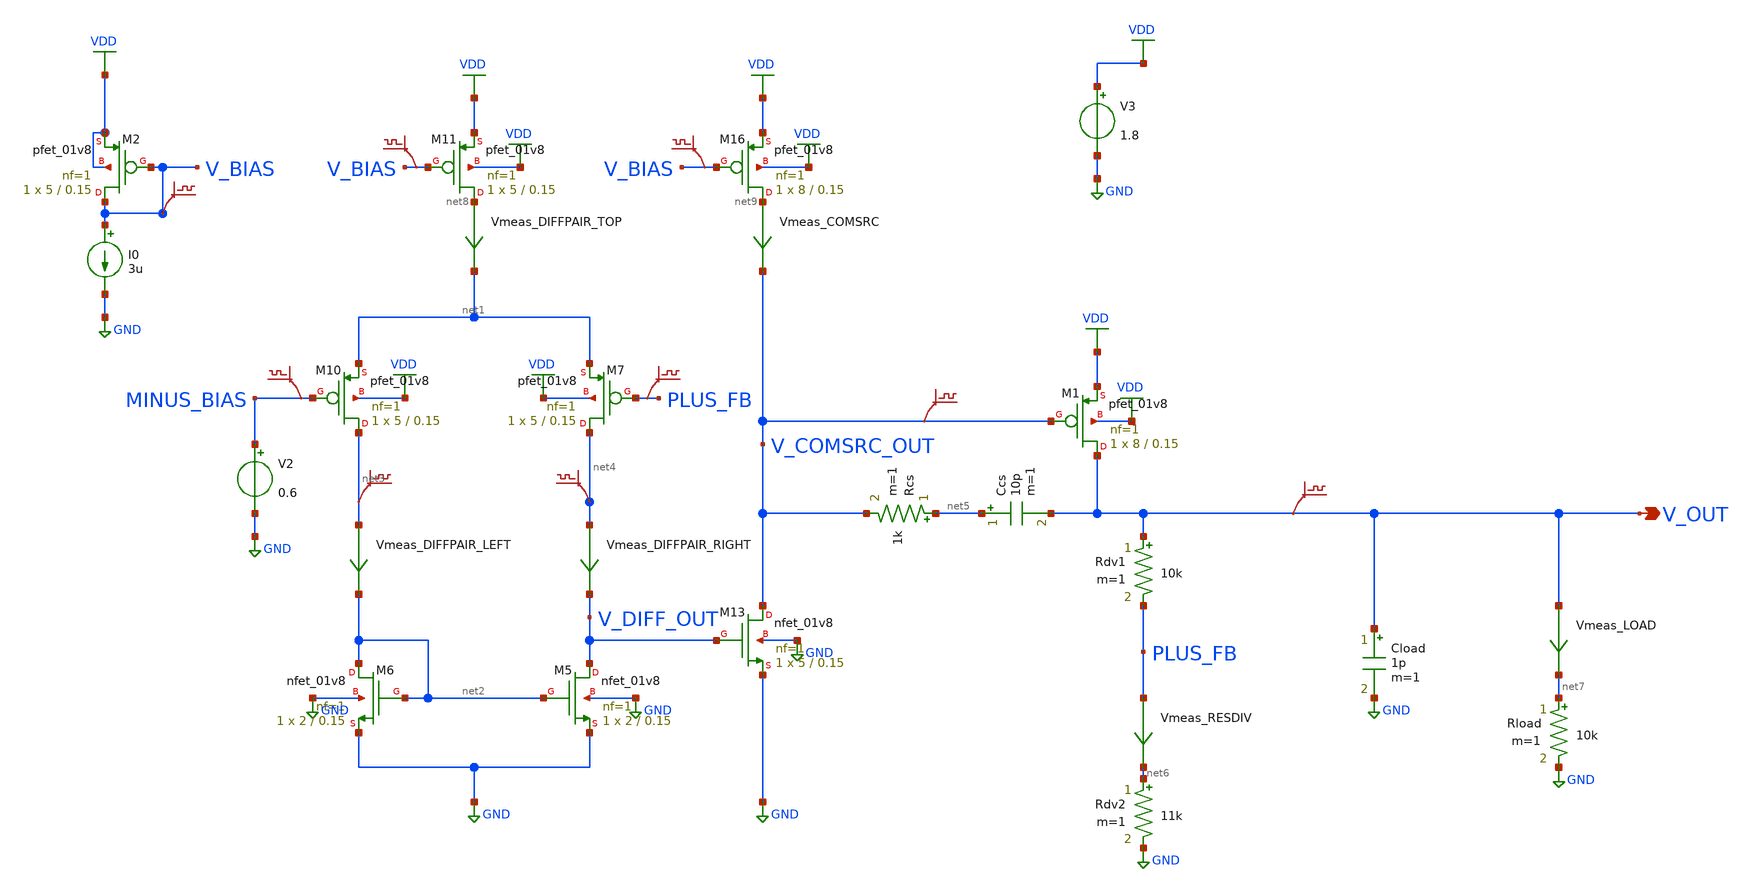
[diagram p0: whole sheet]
** sch_path: lib/xschem/LDO/LDO.sch
**.subckt LDO V_OUT
*.opin V_OUT
XM6 net2 net2 GND GND sky130_fd_pr__nfet_01v8 L=0.15 W=2 nf=1 ad='int((nf+1)/2) * W/nf * 0.29' as='int((nf+2)/2) * W/nf * 0.29'
+ pd='2*int((nf+1)/2) * (W/nf + 0.29)' ps='2*int((nf+2)/2) * (W/nf + 0.29)' nrd='0.29 / W' nrs='0.29 / W'
+ sa=0 sb=0 sd=0 mult=1 m=1
XM5 V_DIFF_OUT net2 GND GND sky130_fd_pr__nfet_01v8 L=0.15 W=2 nf=1 ad='int((nf+1)/2) * W/nf * 0.29'
+ as='int((nf+2)/2) * W/nf * 0.29' pd='2*int((nf+1)/2) * (W/nf + 0.29)' ps='2*int((nf+2)/2) * (W/nf + 0.29)'
+ nrd='0.29 / W' nrs='0.29 / W' sa=0 sb=0 sd=0 mult=1 m=1
XM7 net4 PLUS_FB net1 VDD sky130_fd_pr__pfet_01v8 L=0.15 W=5 nf=1 ad='int((nf+1)/2) * W/nf * 0.29' as='int((nf+2)/2) * W/nf * 0.29'
+ pd='2*int((nf+1)/2) * (W/nf + 0.29)' ps='2*int((nf+2)/2) * (W/nf + 0.29)' nrd='0.29 / W' nrs='0.29 / W'
+ sa=0 sb=0 sd=0 mult=1 m=1
XM10 net3 MINUS_BIAS net1 VDD sky130_fd_pr__pfet_01v8 L=0.15 W=5 nf=1 ad='int((nf+1)/2) * W/nf * 0.29'
+ as='int((nf+2)/2) * W/nf * 0.29' pd='2*int((nf+1)/2) * (W/nf + 0.29)' ps='2*int((nf+2)/2) * (W/nf + 0.29)'
+ nrd='0.29 / W' nrs='0.29 / W' sa=0 sb=0 sd=0 mult=1 m=1
XM11 net8 V_BIAS VDD VDD sky130_fd_pr__pfet_01v8 L=0.15 W=5 nf=1 ad='int((nf+1)/2) * W/nf * 0.29' as='int((nf+2)/2) * W/nf * 0.29'
+ pd='2*int((nf+1)/2) * (W/nf + 0.29)' ps='2*int((nf+2)/2) * (W/nf + 0.29)' nrd='0.29 / W' nrs='0.29 / W'
+ sa=0 sb=0 sd=0 mult=1 m=1
XM13 V_COMSRC_OUT V_DIFF_OUT GND GND sky130_fd_pr__nfet_01v8 L=0.15 W=5 nf=1 ad='int((nf+1)/2) * W/nf * 0.29'
+ as='int((nf+2)/2) * W/nf * 0.29' pd='2*int((nf+1)/2) * (W/nf + 0.29)' ps='2*int((nf+2)/2) * (W/nf + 0.29)'
+ nrd='0.29 / W' nrs='0.29 / W' sa=0 sb=0 sd=0 mult=1 m=1
XM16 net9 V_BIAS VDD VDD sky130_fd_pr__pfet_01v8 L=0.15 W=8 nf=1 ad='int((nf+1)/2) * W/nf * 0.29' as='int((nf+2)/2) * W/nf * 0.29'
+ pd='2*int((nf+1)/2) * (W/nf + 0.29)' ps='2*int((nf+2)/2) * (W/nf + 0.29)' nrd='0.29 / W' nrs='0.29 / W'
+ sa=0 sb=0 sd=0 mult=1 m=1
V2 MINUS_BIAS GND 0.6
V3 VDD GND 1.8
.save v(plus_fb)
.save v(minus_bias)
.save v(net4)
.save v(net3)
.save v(v_comsrc_out)
Vmeas_DIFFPAIR_LEFT net3 net2 0
.save i(vmeas_diffpair_left)
Vmeas_DIFFPAIR_RIGHT net4 V_DIFF_OUT 0
.save i(vmeas_diffpair_right)
Vmeas_COMSRC net9 V_COMSRC_OUT 0
.save i(vmeas_comsrc)
.save v(v_bias)
.save v(v_bias)
Rdv1 V_OUT PLUS_FB 10k m=1
Rdv2 net6 GND 11k m=1
Vmeas_RESDIV PLUS_FB net6 0
.save i(vmeas_resdiv)
Vmeas_DIFFPAIR_TOP net8 net1 0
.save i(vmeas_diffpair_top)
XM2 V_BIAS V_BIAS VDD VDD sky130_fd_pr__pfet_01v8 L=0.15 W=5 nf=1 ad='int((nf+1)/2) * W/nf * 0.29' as='int((nf+2)/2) * W/nf * 0.29'
+ pd='2*int((nf+1)/2) * (W/nf + 0.29)' ps='2*int((nf+2)/2) * (W/nf + 0.29)' nrd='0.29 / W' nrs='0.29 / W'
+ sa=0 sb=0 sd=0 mult=1 m=1
I0 V_BIAS GND 3u
Rcs net5 V_COMSRC_OUT 1k m=1
Ccs net5 V_OUT 10p m=1
Cload V_OUT GND 1p m=1
XM1 V_OUT V_COMSRC_OUT VDD VDD sky130_fd_pr__pfet_01v8 L=0.15 W=8 nf=1 ad='int((nf+1)/2) * W/nf * 0.29'
+ as='int((nf+2)/2) * W/nf * 0.29' pd='2*int((nf+1)/2) * (W/nf + 0.29)' ps='2*int((nf+2)/2) * (W/nf + 0.29)'
+ nrd='0.29 / W' nrs='0.29 / W' sa=0 sb=0 sd=0 mult=1 m=1
Rload net7 GND 10k m=1
.save v(v_bias)
Vmeas_LOAD V_OUT net7 0
.save i(vmeas_load)
.save v(v_out)
**** begin user architecture code

.lib $::SKYWATER_MODELS/sky130.lib.spice tt


**** end user architecture code
**.ends
.GLOBAL VDD
.GLOBAL GND
**** begin user architecture code


.save all
.op
.dc V3 1 2 0.1


**** end user architecture code
.end
